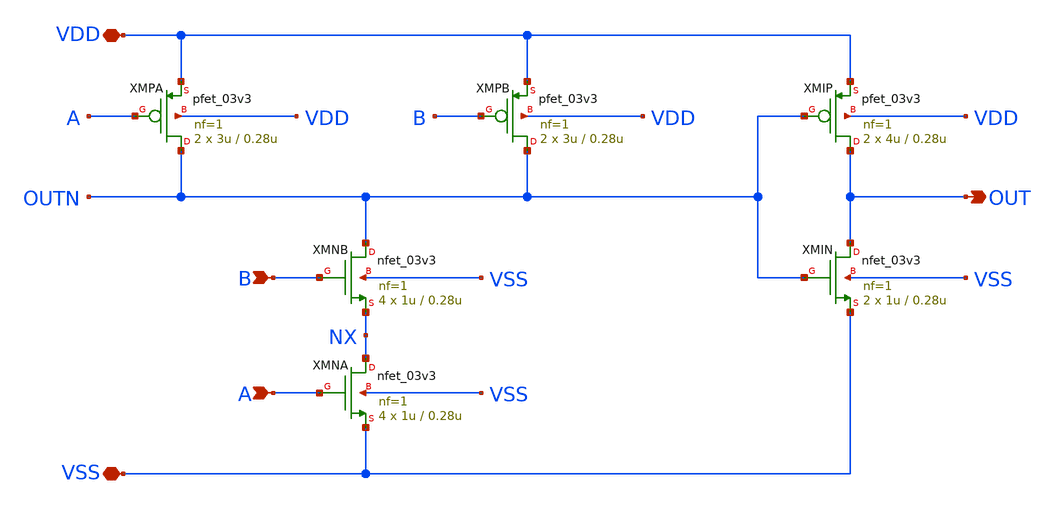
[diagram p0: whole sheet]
** sch_path: designs/DS_modulator/gate_and/xschem/gate_and.sch
**.subckt gate_and OUT A VDD VSS B
*.opin OUT
*.ipin A
*.iopin VDD
*.iopin VSS
*.ipin B
XMNB OUTN B NX VSS nfet_03v3 L=0.28u W=1u nf=1 ad='int((nf+1)/2) * W/nf * 0.18u' as='int((nf+2)/2) * W/nf * 0.18u'
+ pd='2*int((nf+1)/2) * (W/nf + 0.18u)' ps='2*int((nf+2)/2) * (W/nf + 0.18u)' nrd='0.18u / W' nrs='0.18u / W'
+ sa=0 sb=0 sd=0 m=4
XMPB OUTN B VDD VDD pfet_03v3 L=0.28u W=3u nf=1 ad='int((nf+1)/2) * W/nf * 0.18u' as='int((nf+2)/2) * W/nf * 0.18u'
+ pd='2*int((nf+1)/2) * (W/nf + 0.18u)' ps='2*int((nf+2)/2) * (W/nf + 0.18u)' nrd='0.18u / W' nrs='0.18u / W'
+ sa=0 sb=0 sd=0 m=2
XMNA NX A VSS VSS nfet_03v3 L=0.28u W=1u nf=1 ad='int((nf+1)/2) * W/nf * 0.18u' as='int((nf+2)/2) * W/nf * 0.18u'
+ pd='2*int((nf+1)/2) * (W/nf + 0.18u)' ps='2*int((nf+2)/2) * (W/nf + 0.18u)' nrd='0.18u / W' nrs='0.18u / W'
+ sa=0 sb=0 sd=0 m=4
XMPA OUTN A VDD VDD pfet_03v3 L=0.28u W=3u nf=1 ad='int((nf+1)/2) * W/nf * 0.18u' as='int((nf+2)/2) * W/nf * 0.18u'
+ pd='2*int((nf+1)/2) * (W/nf + 0.18u)' ps='2*int((nf+2)/2) * (W/nf + 0.18u)' nrd='0.18u / W' nrs='0.18u / W'
+ sa=0 sb=0 sd=0 m=2
XMIN OUT OUTN VSS VSS nfet_03v3 L=0.28u W=1u nf=1 ad='int((nf+1)/2) * W/nf * 0.18u' as='int((nf+2)/2) * W/nf * 0.18u'
+ pd='2*int((nf+1)/2) * (W/nf + 0.18u)' ps='2*int((nf+2)/2) * (W/nf + 0.18u)' nrd='0.18u / W' nrs='0.18u / W'
+ sa=0 sb=0 sd=0 m=2
XMIP OUT OUTN VDD VDD pfet_03v3 L=0.28u W=4u nf=1 ad='int((nf+1)/2) * W/nf * 0.18u' as='int((nf+2)/2) * W/nf * 0.18u'
+ pd='2*int((nf+1)/2) * (W/nf + 0.18u)' ps='2*int((nf+2)/2) * (W/nf + 0.18u)' nrd='0.18u / W' nrs='0.18u / W'
+ sa=0 sb=0 sd=0 m=2
**.ends
.end
